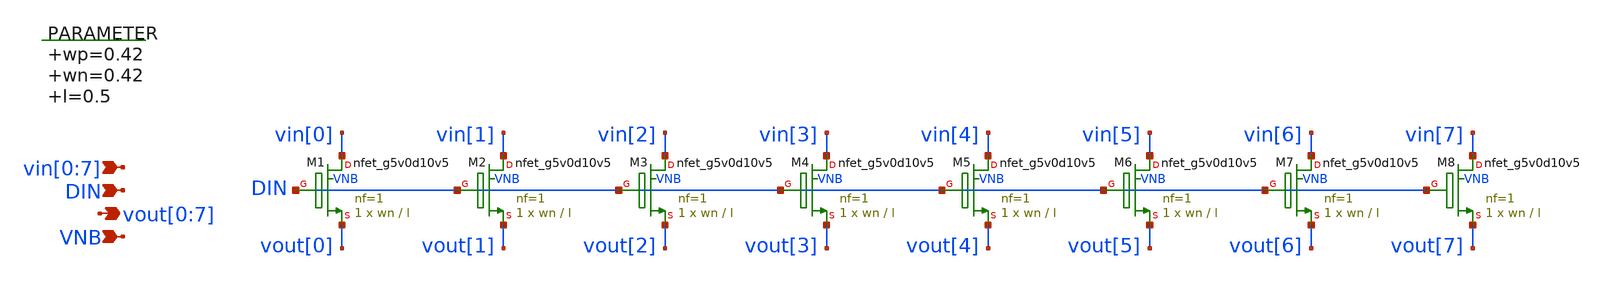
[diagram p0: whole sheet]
** sch_path: xschem/switch_nmos_1g_8o.sch
**.subckt switch_nmos_1g_8o vin[0],vin[1],vin[2],vin[3],vin[4],vin[5],vin[6],vin[7]
*+ vout[0],vout[1],vout[2],vout[3],vout[4],vout[5],vout[6],vout[7] VNB DIN
*.ipin vin[0],vin[1],vin[2],vin[3],vin[4],vin[5],vin[6],vin[7]
*.opin vout[0],vout[1],vout[2],vout[3],vout[4],vout[5],vout[6],vout[7]
*.ipin VNB
*.ipin DIN
.param wp=0.42 wn=0.42 l=0.5

XM1 vin[0] DIN vout[0] VNB sky130_fd_pr__nfet_g5v0d10v5 L=l W=wn nf=1 ad='int((nf+1)/2) * W/nf * 0.29'
+ as='int((nf+2)/2) * W/nf * 0.29' pd='2*int((nf+1)/2) * (W/nf + 0.29)' ps='2*int((nf+2)/2) * (W/nf + 0.29)'
+ nrd='0.29 / W' nrs='0.29 / W' sa=0 sb=0 sd=0 mult=1 m=1
XM2 vin[1] DIN vout[1] VNB sky130_fd_pr__nfet_g5v0d10v5 L=l W=wn nf=1 ad='int((nf+1)/2) * W/nf * 0.29'
+ as='int((nf+2)/2) * W/nf * 0.29' pd='2*int((nf+1)/2) * (W/nf + 0.29)' ps='2*int((nf+2)/2) * (W/nf + 0.29)'
+ nrd='0.29 / W' nrs='0.29 / W' sa=0 sb=0 sd=0 mult=1 m=1
XM3 vin[2] DIN vout[2] VNB sky130_fd_pr__nfet_g5v0d10v5 L=l W=wn nf=1 ad='int((nf+1)/2) * W/nf * 0.29'
+ as='int((nf+2)/2) * W/nf * 0.29' pd='2*int((nf+1)/2) * (W/nf + 0.29)' ps='2*int((nf+2)/2) * (W/nf + 0.29)'
+ nrd='0.29 / W' nrs='0.29 / W' sa=0 sb=0 sd=0 mult=1 m=1
XM4 vin[3] DIN vout[3] VNB sky130_fd_pr__nfet_g5v0d10v5 L=l W=wn nf=1 ad='int((nf+1)/2) * W/nf * 0.29'
+ as='int((nf+2)/2) * W/nf * 0.29' pd='2*int((nf+1)/2) * (W/nf + 0.29)' ps='2*int((nf+2)/2) * (W/nf + 0.29)'
+ nrd='0.29 / W' nrs='0.29 / W' sa=0 sb=0 sd=0 mult=1 m=1
XM5 vin[4] DIN vout[4] VNB sky130_fd_pr__nfet_g5v0d10v5 L=l W=wn nf=1 ad='int((nf+1)/2) * W/nf * 0.29'
+ as='int((nf+2)/2) * W/nf * 0.29' pd='2*int((nf+1)/2) * (W/nf + 0.29)' ps='2*int((nf+2)/2) * (W/nf + 0.29)'
+ nrd='0.29 / W' nrs='0.29 / W' sa=0 sb=0 sd=0 mult=1 m=1
XM6 vin[5] DIN vout[5] VNB sky130_fd_pr__nfet_g5v0d10v5 L=l W=wn nf=1 ad='int((nf+1)/2) * W/nf * 0.29'
+ as='int((nf+2)/2) * W/nf * 0.29' pd='2*int((nf+1)/2) * (W/nf + 0.29)' ps='2*int((nf+2)/2) * (W/nf + 0.29)'
+ nrd='0.29 / W' nrs='0.29 / W' sa=0 sb=0 sd=0 mult=1 m=1
XM7 vin[6] DIN vout[6] VNB sky130_fd_pr__nfet_g5v0d10v5 L=l W=wn nf=1 ad='int((nf+1)/2) * W/nf * 0.29'
+ as='int((nf+2)/2) * W/nf * 0.29' pd='2*int((nf+1)/2) * (W/nf + 0.29)' ps='2*int((nf+2)/2) * (W/nf + 0.29)'
+ nrd='0.29 / W' nrs='0.29 / W' sa=0 sb=0 sd=0 mult=1 m=1
XM8 vin[7] DIN vout[7] VNB sky130_fd_pr__nfet_g5v0d10v5 L=l W=wn nf=1 ad='int((nf+1)/2) * W/nf * 0.29'
+ as='int((nf+2)/2) * W/nf * 0.29' pd='2*int((nf+1)/2) * (W/nf + 0.29)' ps='2*int((nf+2)/2) * (W/nf + 0.29)'
+ nrd='0.29 / W' nrs='0.29 / W' sa=0 sb=0 sd=0 mult=1 m=1
**.ends
.end
